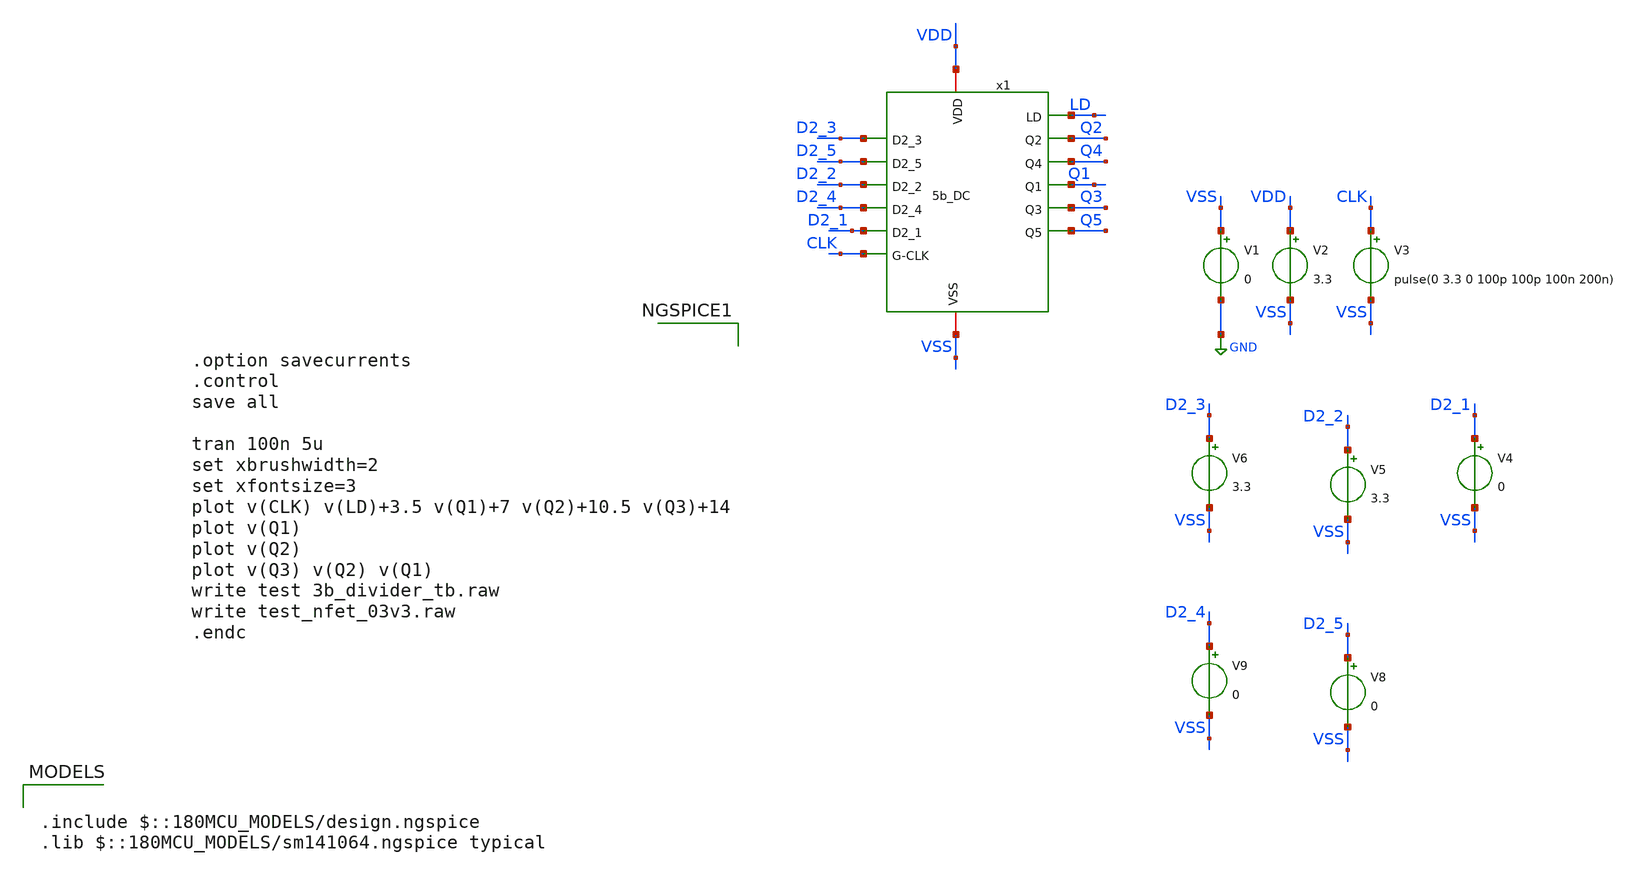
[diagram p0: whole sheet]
** sch_path: Clock_Generator_PAKISTAN_06/Schematics/5b_DC_tb.sch
**.subckt 5b_DC_tb
V1 VSS GND 0
V2 VDD VSS 3.3
V3 CLK VSS pulse(0 3.3 0 100p 100p 100n 200n)
V4 D2_1 VSS 0
V5 D2_2 VSS 3.3
V6 D2_3 VSS 3.3
V8 D2_5 VSS 0
V9 D2_4 VSS 0
x1 LD VDD Q2 Q4 Q1 Q3 Q5 D2_3 D2_5 D2_2 D2_4 D2_1 CLK VSS 5b_DC
**** begin user architecture code


.option savecurrents
.control
save all

tran 100n 5u
set xbrushwidth=2
set xfontsize=3
plot v(CLK) v(LD)+3.5 v(Q1)+7 v(Q2)+10.5 v(Q3)+14
plot v(Q1)
plot v(Q2)
plot v(Q3) v(Q2) v(Q1)
write test 3b_divider_tb.raw
write test_nfet_03v3.raw
.endc



.include $::180MCU_MODELS/design.ngspice
.lib $::180MCU_MODELS/sm141064.ngspice typical

**** end user architecture code
**.ends
.GLOBAL GND
.end
